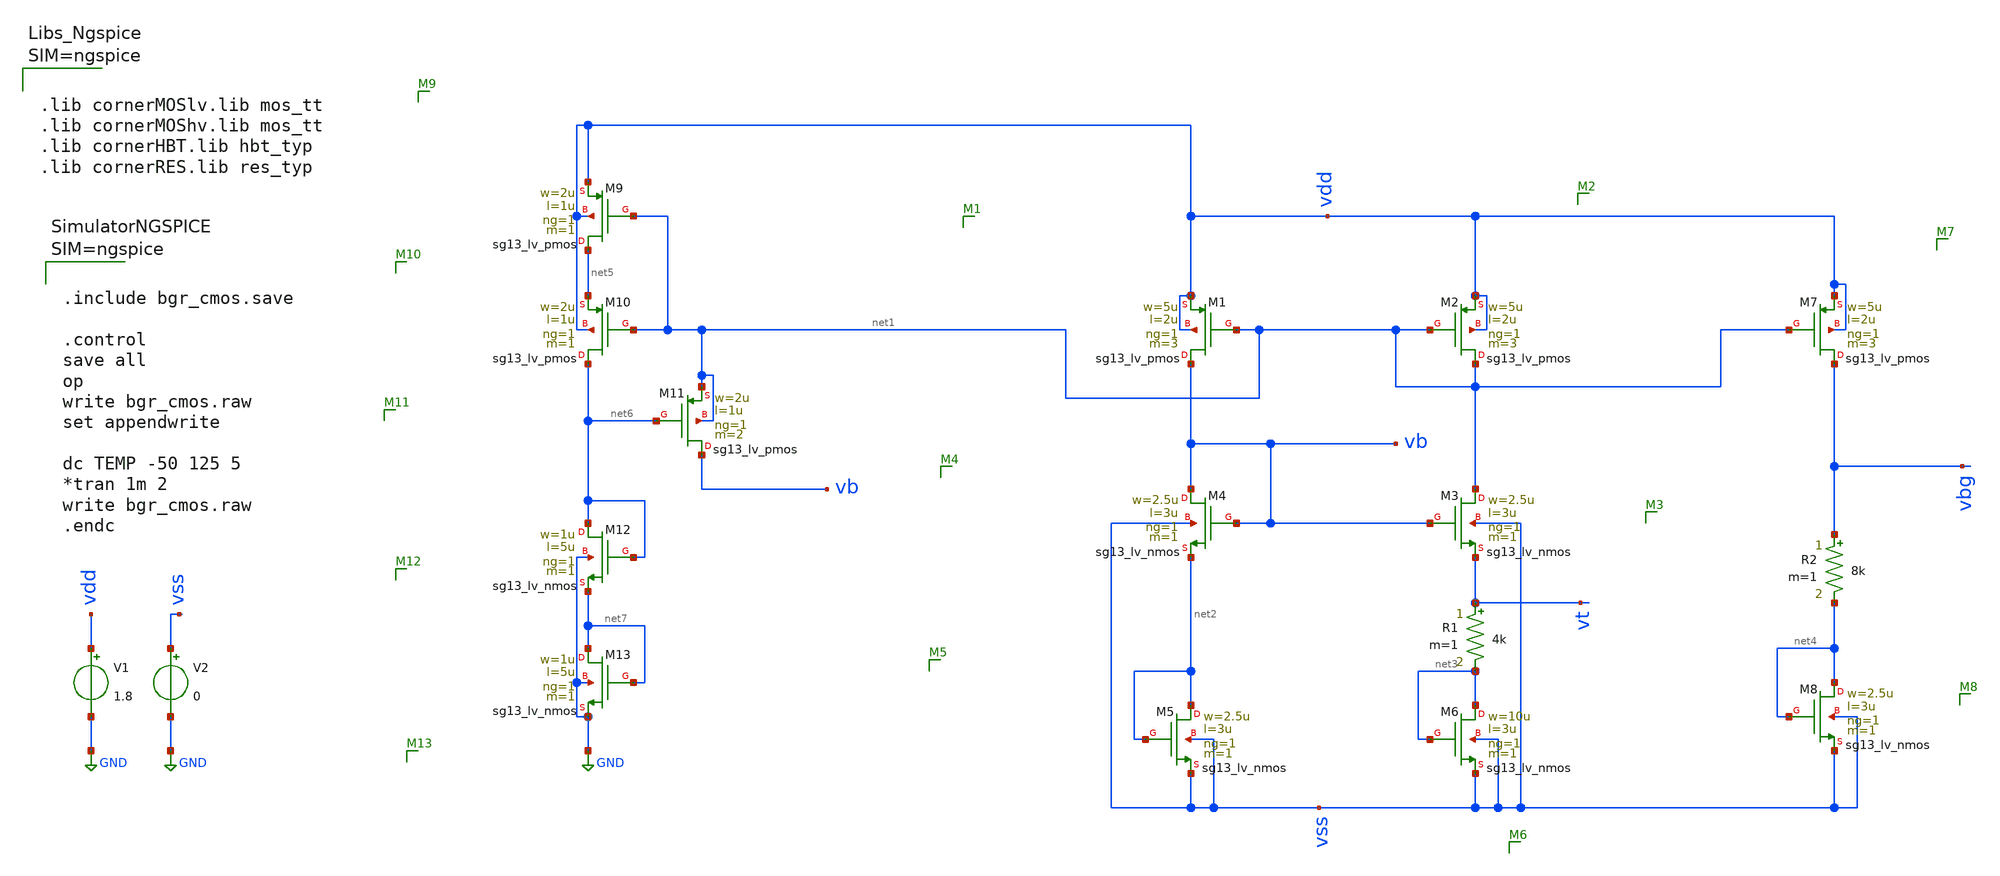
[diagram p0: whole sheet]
** sch_path: Schematics/ali_designs/bgr_cmos.sch
**.subckt bgr_cmos
XM1 vb net1 vdd vdd sg13_lv_pmos w=5u l=2u ng=1 m=3 mm_ok=1
XM2 net1 net1 vdd vdd sg13_lv_pmos w=5u l=2u ng=1 m=3 mm_ok=1
XM3 net1 vb vt vss sg13_lv_nmos w=2.5u l=3u ng=1 m=1 mm_ok=1
XM4 vb vb net2 vss sg13_lv_nmos w=2.5u l=3u ng=1 m=1 mm_ok=1
V1 vdd GND 1.8
V2 vss GND 0
XM5 net2 net2 vss vss sg13_lv_nmos w=2.5u l=3u ng=1 m=1 mm_ok=1
R1 vt net3 4k m=1
XM6 net3 net3 vss vss sg13_lv_nmos w=10u l=3u ng=1 m=1 mm_ok=1
XM7 vbg net1 vdd vdd sg13_lv_pmos w=5u l=2u ng=1 m=3 mm_ok=1
XM8 net4 net4 vss vss sg13_lv_nmos w=2.5u l=3u ng=1 m=1 mm_ok=1
R2 vbg net4 8k m=1
XM9 net5 net1 vdd vdd sg13_lv_pmos w=2u l=1u ng=1 m=1 mm_ok=1
XM10 net6 net1 net5 vdd sg13_lv_pmos w=2u l=1u ng=1 m=1 mm_ok=1
XM11 vb net6 net1 net1 sg13_lv_pmos w=2u l=1u ng=1 m=2 mm_ok=1
XM12 net6 net6 net7 GND sg13_lv_nmos w=1u l=5u ng=1 m=1 mm_ok=1
XM13 net7 net7 GND GND sg13_lv_nmos w=1u l=5u ng=1 m=1 mm_ok=1
**** begin user architecture code



.include bgr_cmos.save

.control
save all
op
write bgr_cmos.raw
set appendwrite

dc TEMP -50 125 5
*tran 1m 2
write bgr_cmos.raw
.endc






.lib cornerMOSlv.lib mos_tt
.lib cornerMOShv.lib mos_tt
.lib cornerHBT.lib hbt_typ
.lib cornerRES.lib res_typ



**** end user architecture code
**.ends
.GLOBAL GND
.end
